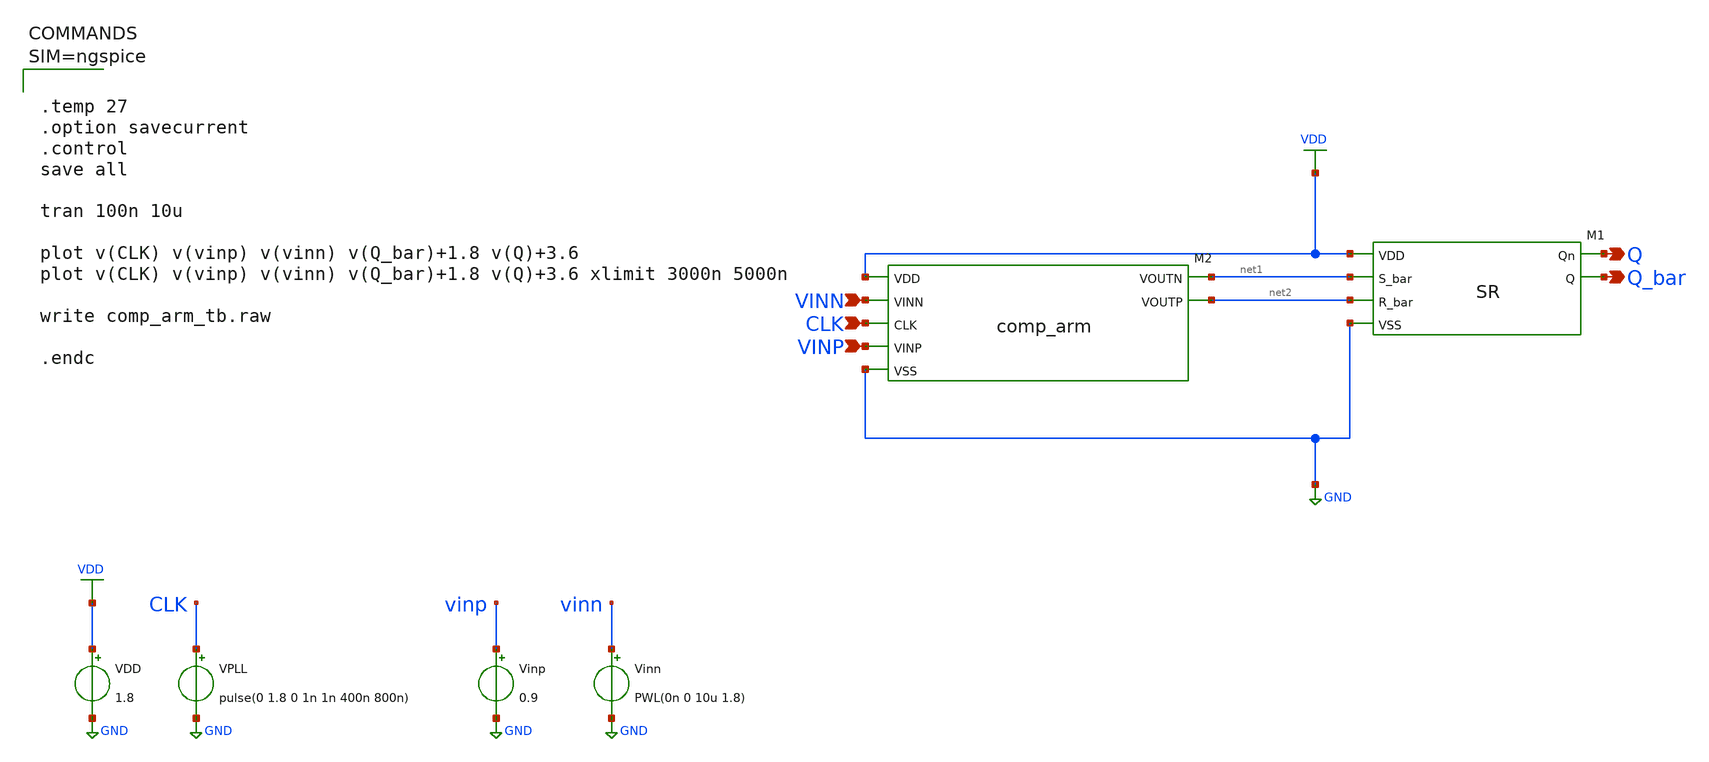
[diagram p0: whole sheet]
** sch_path: SKY130/SAR-ADC/SAR-ADC_1.8V/comp_arm_tb.sch
**.subckt comp_arm_tb CLK VINP VINN Q Q_bar
*.ipin CLK
*.ipin VINP
*.ipin VINN
*.opin Q
*.opin Q_bar
XM1 VDD Q Q_bar net2 net1 GND SR
XM2 net2 VDD VINP VINN CLK GND net1 comp_arm
VDD VDD GND 1.8
Vinn vinn GND PWL(0n 0 10u 1.8)
Vinp vinp GND 0.9
VPLL CLK GND pulse(0 1.8 0 1n 1n 400n 800n)
**** begin user architecture code

** opencircuitdesign pdks install
.lib $::SKYWATER_MODELS/sky130.lib.spice tt




.temp 27
.option savecurrent
.control
save all

tran 100n 10u

plot v(CLK) v(vinp) v(vinn) v(Q_bar)+1.8 v(Q)+3.6
plot v(CLK) v(vinp) v(vinn) v(Q_bar)+1.8 v(Q)+3.6 xlimit 3000n 5000n

write comp_arm_tb.raw

.endc



**** end user architecture code
**.ends

* expanding   symbol:  SR.sym # of pins=6
** sym_path: SKY130/SAR-ADC/SAR-ADC_5.0V/SR.sym
** sch_path: SKY130/SAR-ADC/SAR-ADC_5.0V/SR.sch
.subckt SR VDD Qn Q R_bar S_bar VSS


*.iopin VDD
*.opin Qn
*.opin Q
*.ipin S_bar
*.ipin R_bar
*.iopin VSS
XM7 Qn Q VDD VDD sky130_fd_pr__pfet_g5v0d10v5 L=0.5 W=6 nf=1 ad='int((1 + 1)/2) * 6 / 1 * 0.29' as='int((1 + 2)/2) * 6 / 1 * 0.29'
+ pd='2*int((1 + 1)/2) * (6 / 1 + 0.29)' ps='2*int((1 + 2)/2) * (6 / 1 + 0.29)' nrd='0.29 / 6 ' nrs='0.29 / 6 '
+ sa=0 sb=0 sd=0 mult=1 m=1
XM8 Qn S_bar VDD VDD sky130_fd_pr__pfet_g5v0d10v5 L=0.5 W=6 nf=1 ad='int((1 + 1)/2) * 6 / 1 * 0.29' as='int((1 + 2)/2) * 6 / 1 * 0.29'
+ pd='2*int((1 + 1)/2) * (6 / 1 + 0.29)' ps='2*int((1 + 2)/2) * (6 / 1 + 0.29)' nrd='0.29 / 6 ' nrs='0.29 / 6 '
+ sa=0 sb=0 sd=0 mult=1 m=1
XM15 Qn S_bar net1 VSS sky130_fd_pr__nfet_g5v0d10v5 L=0.5 W=3 nf=1 ad='int((1 + 1)/2) * 3 / 1 * 0.29'
+ as='int((1 + 2)/2) * 3 / 1 * 0.29' pd='2*int((1 + 1)/2) * (3 / 1 + 0.29)' ps='2*int((1 + 2)/2) * (3 / 1 + 0.29)'
+ nrd='0.29 / 3 ' nrs='0.29 / 3 ' sa=0 sb=0 sd=0 mult=1 m=1
XM16 net1 Q VSS VSS sky130_fd_pr__nfet_g5v0d10v5 L=0.5 W=3 nf=1 ad='int((1 + 1)/2) * 3 / 1 * 0.29' as='int((1 + 2)/2) * 3 / 1 * 0.29'
+ pd='2*int((1 + 1)/2) * (3 / 1 + 0.29)' ps='2*int((1 + 2)/2) * (3 / 1 + 0.29)' nrd='0.29 / 3 ' nrs='0.29 / 3 '
+ sa=0 sb=0 sd=0 mult=1 m=1
XM17 Q R_bar VDD VDD sky130_fd_pr__pfet_g5v0d10v5 L=0.5 W=6 nf=1 ad='int((1 + 1)/2) * 6 / 1 * 0.29' as='int((1 + 2)/2) * 6 / 1 * 0.29'
+ pd='2*int((1 + 1)/2) * (6 / 1 + 0.29)' ps='2*int((1 + 2)/2) * (6 / 1 + 0.29)' nrd='0.29 / 6 ' nrs='0.29 / 6 '
+ sa=0 sb=0 sd=0 mult=1 m=1
XM18 Q Qn VDD VDD sky130_fd_pr__pfet_g5v0d10v5 L=0.5 W=6 nf=1 ad='int((1 + 1)/2) * 6 / 1 * 0.29' as='int((1 + 2)/2) * 6 / 1 * 0.29'
+ pd='2*int((1 + 1)/2) * (6 / 1 + 0.29)' ps='2*int((1 + 2)/2) * (6 / 1 + 0.29)' nrd='0.29 / 6 ' nrs='0.29 / 6 '
+ sa=0 sb=0 sd=0 mult=1 m=1
XM23 Q Qn net2 VSS sky130_fd_pr__nfet_g5v0d10v5 L=0.5 W=3 nf=1 ad='int((1 + 1)/2) * 3 / 1 * 0.29' as='int((1 + 2)/2) * 3 / 1 * 0.29'
+ pd='2*int((1 + 1)/2) * (3 / 1 + 0.29)' ps='2*int((1 + 2)/2) * (3 / 1 + 0.29)' nrd='0.29 / 3 ' nrs='0.29 / 3 '
+ sa=0 sb=0 sd=0 mult=1 m=1
XM27 net2 R_bar VSS VSS sky130_fd_pr__nfet_g5v0d10v5 L=0.5 W=3 nf=1 ad='int((1 + 1)/2) * 3 / 1 * 0.29'
+ as='int((1 + 2)/2) * 3 / 1 * 0.29' pd='2*int((1 + 1)/2) * (3 / 1 + 0.29)' ps='2*int((1 + 2)/2) * (3 / 1 + 0.29)'
+ nrd='0.29 / 3 ' nrs='0.29 / 3 ' sa=0 sb=0 sd=0 mult=1 m=1
.ends


* expanding   symbol:  comp_arm.sym # of pins=7
** sym_path: SKY130/SAR-ADC/SAR-ADC_1.8V/comp_arm.sym
** sch_path: SKY130/SAR-ADC/SAR-ADC_1.8V/comp_arm.sch
.subckt comp_arm VOUTP VDD VINP VINN CLK VSS VOUTN

*.iopin VSS
*.iopin VDD
*.ipin CLK
*.ipin VINP
*.ipin VINN
*.opin VOUTN
*.opin VOUTP
XM1 net1 CLK VDD VDD sky130_fd_pr__pfet_01v8 L=0.15 W=15 nf=1 ad='int((1 + 1)/2) * 15 / 1 * 0.29' as='int((1 + 2)/2) * 15 / 1 * 0.29'
+ pd='2*int((1 + 1)/2) * (15 / 1 + 0.29)' ps='2*int((1 + 2)/2) * (15 / 1 + 0.29)' nrd='0.29 / 15 ' nrs='0.29 / 15 '
+ sa=0 sb=0 sd=0 mult=1 m=1
XM2 VOUTN CLK VDD VDD sky130_fd_pr__pfet_01v8 L=0.15 W=15 nf=1 ad='int((1 + 1)/2) * 15 / 1 * 0.29' as='int((1 + 2)/2) * 15 / 1 * 0.29'
+ pd='2*int((1 + 1)/2) * (15 / 1 + 0.29)' ps='2*int((1 + 2)/2) * (15 / 1 + 0.29)' nrd='0.29 / 15 ' nrs='0.29 / 15 '
+ sa=0 sb=0 sd=0 mult=1 m=1
XM3 VOUTN VOUTP VDD VDD sky130_fd_pr__pfet_01v8 L=0.15 W=15 nf=1 ad='int((1 + 1)/2) * 15 / 1 * 0.29'
+ as='int((1 + 2)/2) * 15 / 1 * 0.29' pd='2*int((1 + 1)/2) * (15 / 1 + 0.29)' ps='2*int((1 + 2)/2) * (15 / 1 + 0.29)'
+ nrd='0.29 / 15 ' nrs='0.29 / 15 ' sa=0 sb=0 sd=0 mult=1 m=1
XM4 VOUTP VOUTN VDD VDD sky130_fd_pr__pfet_01v8 L=0.15 W=15 nf=1 ad='int((1 + 1)/2) * 15 / 1 * 0.29'
+ as='int((1 + 2)/2) * 15 / 1 * 0.29' pd='2*int((1 + 1)/2) * (15 / 1 + 0.29)' ps='2*int((1 + 2)/2) * (15 / 1 + 0.29)'
+ nrd='0.29 / 15 ' nrs='0.29 / 15 ' sa=0 sb=0 sd=0 mult=1 m=1
XM5 VOUTP CLK VDD VDD sky130_fd_pr__pfet_01v8 L=0.15 W=15 nf=1 ad='int((1 + 1)/2) * 15 / 1 * 0.29' as='int((1 + 2)/2) * 15 / 1 * 0.29'
+ pd='2*int((1 + 1)/2) * (15 / 1 + 0.29)' ps='2*int((1 + 2)/2) * (15 / 1 + 0.29)' nrd='0.29 / 15 ' nrs='0.29 / 15 '
+ sa=0 sb=0 sd=0 mult=1 m=1
XM6 net2 CLK VDD VDD sky130_fd_pr__pfet_01v8 L=0.15 W=15 nf=1 ad='int((1 + 1)/2) * 15 / 1 * 0.29' as='int((1 + 2)/2) * 15 / 1 * 0.29'
+ pd='2*int((1 + 1)/2) * (15 / 1 + 0.29)' ps='2*int((1 + 2)/2) * (15 / 1 + 0.29)' nrd='0.29 / 15 ' nrs='0.29 / 15 '
+ sa=0 sb=0 sd=0 mult=1 m=1
XM7 VOUTN VOUTP net1 VSS sky130_fd_pr__nfet_01v8 L=0.15 W=5 nf=1 ad='int((1 + 1)/2) * 5 / 1 * 0.29' as='int((1 + 2)/2) * 5 / 1 * 0.29'
+ pd='2*int((1 + 1)/2) * (5 / 1 + 0.29)' ps='2*int((1 + 2)/2) * (5 / 1 + 0.29)' nrd='0.29 / 5 ' nrs='0.29 / 5 '
+ sa=0 sb=0 sd=0 mult=1 m=1
XM10 net2 VINN net3 VSS sky130_fd_pr__nfet_01v8 L=0.15 W=5 nf=1 ad='int((1 + 1)/2) * 5 / 1 * 0.29' as='int((1 + 2)/2) * 5 / 1 * 0.29'
+ pd='2*int((1 + 1)/2) * (5 / 1 + 0.29)' ps='2*int((1 + 2)/2) * (5 / 1 + 0.29)' nrd='0.29 / 5 ' nrs='0.29 / 5 '
+ sa=0 sb=0 sd=0 mult=1 m=1
XM8 VOUTP VOUTN net2 VSS sky130_fd_pr__nfet_01v8 L=0.15 W=5 nf=1 ad='int((1 + 1)/2) * 5 / 1 * 0.29' as='int((1 + 2)/2) * 5 / 1 * 0.29'
+ pd='2*int((1 + 1)/2) * (5 / 1 + 0.29)' ps='2*int((1 + 2)/2) * (5 / 1 + 0.29)' nrd='0.29 / 5 ' nrs='0.29 / 5 '
+ sa=0 sb=0 sd=0 mult=1 m=1
XM9 net1 VINP net3 VSS sky130_fd_pr__nfet_01v8 L=0.15 W=5 nf=1 ad='int((1 + 1)/2) * 5 / 1 * 0.29' as='int((1 + 2)/2) * 5 / 1 * 0.29'
+ pd='2*int((1 + 1)/2) * (5 / 1 + 0.29)' ps='2*int((1 + 2)/2) * (5 / 1 + 0.29)' nrd='0.29 / 5 ' nrs='0.29 / 5 '
+ sa=0 sb=0 sd=0 mult=1 m=1
XM11 net3 CLK VSS VSS sky130_fd_pr__nfet_01v8 L=0.15 W=5 nf=1 ad='int((1 + 1)/2) * 5 / 1 * 0.29' as='int((1 + 2)/2) * 5 / 1 * 0.29'
+ pd='2*int((1 + 1)/2) * (5 / 1 + 0.29)' ps='2*int((1 + 2)/2) * (5 / 1 + 0.29)' nrd='0.29 / 5 ' nrs='0.29 / 5 '
+ sa=0 sb=0 sd=0 mult=1 m=1
.ends

.GLOBAL VDD
.GLOBAL GND
.end
